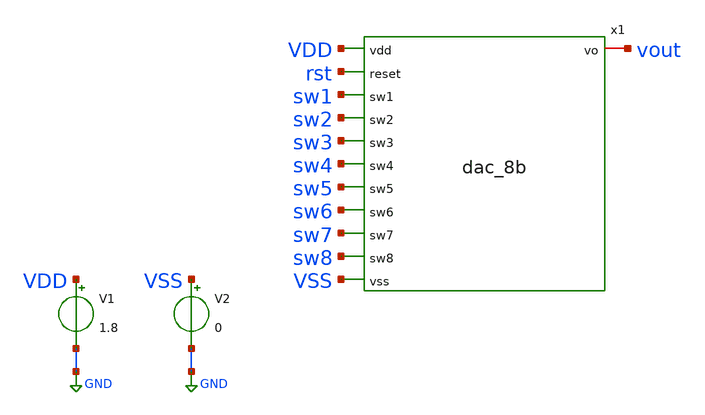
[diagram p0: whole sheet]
** sch_path: xschem/dac_tb.sch
**.subckt dac_tb
x1 VDD rst sw1 sw2 sw3 sw4 sw5 sw6 sw7 sw8 VSS vout dac_8b
V1 VDD GND 1.8
V2 VSS GND 0
**** begin user architecture code

.options acct list
.temp 25
v_rst rst VSS  PULSE(0 1.8V 0 50p 50p 10us 1280us)
v_s1 sw8 VSS  PULSE(0 1.8V 0 50p 50p 5us 1280us)
v_s2 sw7 VSS  PULSE(0 1.8V 0 50p 50p 15us 1280us)
v_s3 sw6 VSS  PULSE(0 1.8V 0 50p 50p 25us 1280us)
v_s4 sw5 VSS  PULSE(0 1.8V 0 50p 50p 45us 1280us)
v_s5 sw4 VSS  PULSE(0 1.8V 0 50p 50p 85us 1280us)
v_s6 sw3 VSS  PULSE(0 1.8V 0 50p 50p 165us 1280us)
v_s7 sw2 VSS  PULSE(0 1.8V 0 50p 50p 325us 1280us)
v_s8 sw1 VSS  PULSE(0 1.8V 0 50p 50p 645us 1280us)

.control
ic v(vout)=1.8V
save all
tran 0.1u 3m
plot sw1 sw2+2 sw2+4 sw3+6 sw4+8 sw5+10 sw6+12 sw7+14 sw8+16 rst+18
plot vout
plot fft(vout) vs frequency
.endc



** opencircuitdesign pdks install
.lib $::SKYWATER_MODELS/sky130.lib.spice tt
.include /usr/local/share/pdk/sky130A/libs.ref/sky130_fd_sc_hd/spice/sky130_fd_sc_hd.spice

**** end user architecture code
**.ends

* expanding   symbol:  /home/mthudaa/Documents/Time_SAR_ADC/xschem/dac_8b.sym # of pins=12
** sym_path: xschem/dac_8b.sym
** sch_path: xschem/dac_8b.sch
.subckt dac_8b vdd reset sw1 sw2 sw3 sw4 sw5 sw6 sw7 sw8 vss vo
*.ipin vdd
*.ipin reset
*.ipin sw1
*.ipin sw2
*.ipin sw3
*.ipin sw4
*.ipin sw5
*.ipin sw6
*.ipin sw7
*.ipin sw8
*.ipin vss
*.iopin vo
x1 net1 net2 net3 net4 net5 net6 net7 net8 vss vo cap_array
x3 vdd sw8 sw7 net1 net2 sw6 sw5 net3 sw4 net4 net5 sw3 net6 sw2 net7 sw1 net8 vss dac_sw_8b
x4 reset vss vss vdd vdd rn sky130_fd_sc_hd__inv_1
x5 rn vss vss vdd vdd rp sky130_fd_sc_hd__inv_1
x2 vdd rp rn vss vss vo tg_sw
.ends


* expanding   symbol:  /home/mthudaa/Documents/Time_SAR_ADC/xschem/cap_array.sym # of pins=10
** sym_path: xschem/cap_array.sym
** sch_path: xschem/cap_array.sch
.subckt cap_array c1 c2 c3 c4 c5 c6 c7 c8 c9 vbuff
*.ipin c1
*.ipin c2
*.ipin c3
*.ipin c4
*.ipin c5
*.ipin c6
*.ipin c7
*.ipin c8
*.ipin c9
*.iopin vbuff
XC1 vbuff c9 sky130_fd_pr__cap_mim_m3_1 W=1 L=1 MF=1 m=1
XC2 vbuff c8 sky130_fd_pr__cap_mim_m3_1 W=1 L=1 MF=1 m=1
XC3 vbuff c7 sky130_fd_pr__cap_mim_m3_1 W=1 L=1 MF=2 m=2
XC4 vbuff c6 sky130_fd_pr__cap_mim_m3_1 W=1 L=1 MF=4 m=4
XC5 vbuff c5 sky130_fd_pr__cap_mim_m3_1 W=1 L=1 MF=8 m=8
XC6 vbuff c4 sky130_fd_pr__cap_mim_m3_1 W=1 L=1 MF=16 m=16
XC7 vbuff c3 sky130_fd_pr__cap_mim_m3_1 W=1 L=1 MF=32 m=32
XC8 vbuff c2 sky130_fd_pr__cap_mim_m3_1 W=1 L=1 MF=64 m=64
XC9 vbuff c1 sky130_fd_pr__cap_mim_m3_1 W=1 L=1 MF=128 m=128
.ends


* expanding   symbol:  /home/mthudaa/Documents/Time_SAR_ADC/xschem/dac_sw_8b.sym # of pins=18
** sym_path: xschem/dac_sw_8b.sym
** sch_path: xschem/dac_sw_8b.sch
.subckt dac_sw_8b vdd sw8 sw7 c1 c2 sw6 sw5 c3 sw4 c4 c5 sw3 c6 sw2 c7 sw1 c8 vss
*.ipin vdd
*.ipin sw8
*.ipin sw7
*.ipin sw6
*.ipin sw5
*.ipin sw4
*.ipin sw3
*.ipin sw2
*.ipin sw1
*.ipin vss
*.opin c8
*.opin c7
*.opin c6
*.opin c5
*.opin c4
*.opin c3
*.opin c2
*.opin c1
x9 sw8 vss vss vdd vdd sky130_fd_sc_hd__diode_2
x10 sw7 vss vss vdd vdd sky130_fd_sc_hd__diode_2
x11 sw6 vss vss vdd vdd sky130_fd_sc_hd__diode_2
x12 sw5 vss vss vdd vdd sky130_fd_sc_hd__diode_2
x13 sw4 vss vss vdd vdd sky130_fd_sc_hd__diode_2
x14 sw3 vss vss vdd vdd sky130_fd_sc_hd__diode_2
x15 sw2 vss vss vdd vdd sky130_fd_sc_hd__diode_2
x16 sw1 vss vss vdd vdd sky130_fd_sc_hd__diode_2
x1 sw8 vss vss vdd vdd c8 sky130_fd_sc_hd__clkinv_16
x2 sw7 vss vss vdd vdd c7 sky130_fd_sc_hd__clkinv_16
x3 sw6 vss vss vdd vdd c6 sky130_fd_sc_hd__clkinv_16
x4 sw5 vss vss vdd vdd c5 sky130_fd_sc_hd__clkinv_16
x5 sw4 vss vss vdd vdd c4 sky130_fd_sc_hd__clkinv_16
x6 sw3 vss vss vdd vdd c3 sky130_fd_sc_hd__clkinv_16
x7 sw2 vss vss vdd vdd c2 sky130_fd_sc_hd__clkinv_16
x8 sw1 vss vss vdd vdd c1 sky130_fd_sc_hd__clkinv_16
.ends


* expanding   symbol:  /home/mthudaa/Documents/Time_SAR_ADC/xschem/tg_sw.sym # of pins=6
** sym_path: xschem/tg_sw.sym
** sch_path: xschem/tg_sw.sch
.subckt tg_sw vdd swp swn vss in out
*.ipin vdd
*.ipin swp
*.ipin swn
*.ipin vss
*.iopin in
*.iopin out
XM1 in swp out vss sky130_fd_pr__nfet_01v8 L=0.15 W=1 nf=1 ad='int((nf+1)/2) * W/nf * 0.29' as='int((nf+2)/2) * W/nf * 0.29'
+ pd='2*int((nf+1)/2) * (W/nf + 0.29)' ps='2*int((nf+2)/2) * (W/nf + 0.29)' nrd='0.29 / W' nrs='0.29 / W'
+ sa=0 sb=0 sd=0 mult=1 m=1
XM2 in swn out vdd sky130_fd_pr__pfet_01v8 L=0.15 W=1.5 nf=1 ad='int((nf+1)/2) * W/nf * 0.29' as='int((nf+2)/2) * W/nf * 0.29'
+ pd='2*int((nf+1)/2) * (W/nf + 0.29)' ps='2*int((nf+2)/2) * (W/nf + 0.29)' nrd='0.29 / W' nrs='0.29 / W'
+ sa=0 sb=0 sd=0 mult=1 m=1
.ends

.GLOBAL GND
.end
